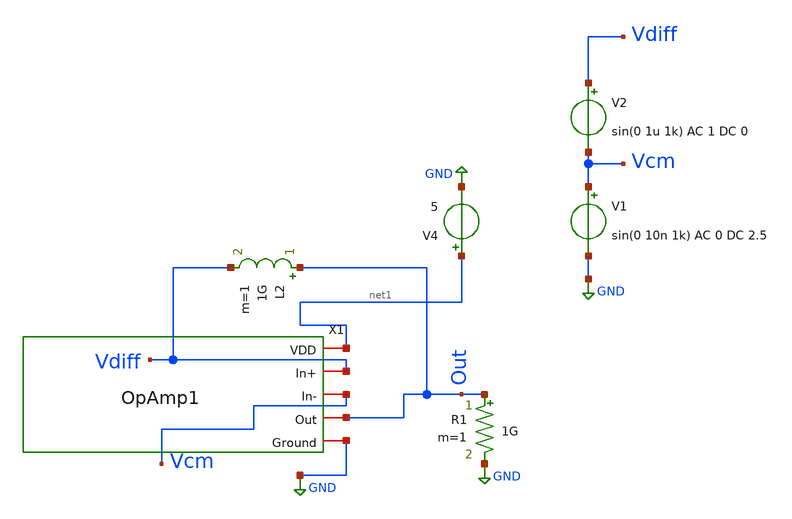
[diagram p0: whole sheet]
** sch_path: xschem/OpAmpTb.sch
**.subckt OpAmpTb
V1 Vcm GND sin(0 10n 1k) AC 0 DC 2.5
V2 Vdiff Vcm sin(0 1u 1k) AC 1 DC 0
V4 net1 GND 5
L2 Out Vdiff 1G m=1
R1 Out GND 1G m=1
X1 net1 Vdiff Vcm Out GND OpAmp1
**** begin user architecture code

* this option enables mos model bin
* selection based on W/NF instead of W
.include ~/Project/mag/OpAmp.spice
*.include ~/Project/mag/CurrentRef.spice
*.include ~/Project/mag/CurRefResistor.spice
*.include ~/Project/mag/ConnectedNMOSPair.spice
*.include ~/Project/mag/NMOSPair.spice
*.include ~/Project/mag/GainStage.spice
*.include ~/Project/mag/DifferentialPair.spice
*.include ~/Project/mag/ConnectedPMOSPair.spice
*.include ~/Project/mag/PMOSPair.spice
.control
op
print all
save all
ac dec 10 1 1G
plot Vdb(Out)


.endc



** opencircuitdesign pdks install
.lib $::SKYWATER_MODELS/sky130.lib.spice tt


**** end user architecture code
**.ends
.GLOBAL GND
.end
